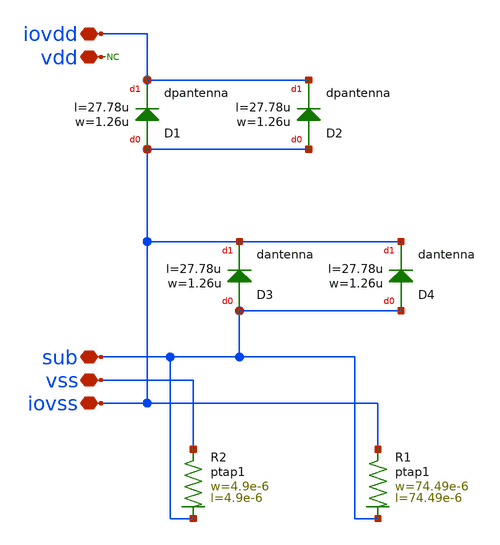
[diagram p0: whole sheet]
** sch_path: ihp-sg13g2/sg13g2_io/xschem/sg13g2_IOPadIOVss.sch
**.subckt sg13g2_IOPadIOVss iovdd vss vdd sub iovss
*.iopin iovdd
*.iopin vss
*.iopin vdd
*.iopin sub
*.iopin iovss
XR2 vss sub ptap1 R=22.47 w=4.9e-6 l=4.9e-6
* noconn vdd
XR1 iovss sub ptap1 R=167.6m w=74.49e-6 l=74.49e-6
XD1 iovss iovdd dpantenna l=27.78u w=1.26u
XD3 sub iovss dantenna l=27.78u w=1.26u
XD2 iovss iovdd dpantenna l=27.78u w=1.26u
XD4 sub iovss dantenna l=27.78u w=1.26u
**.ends
.end
